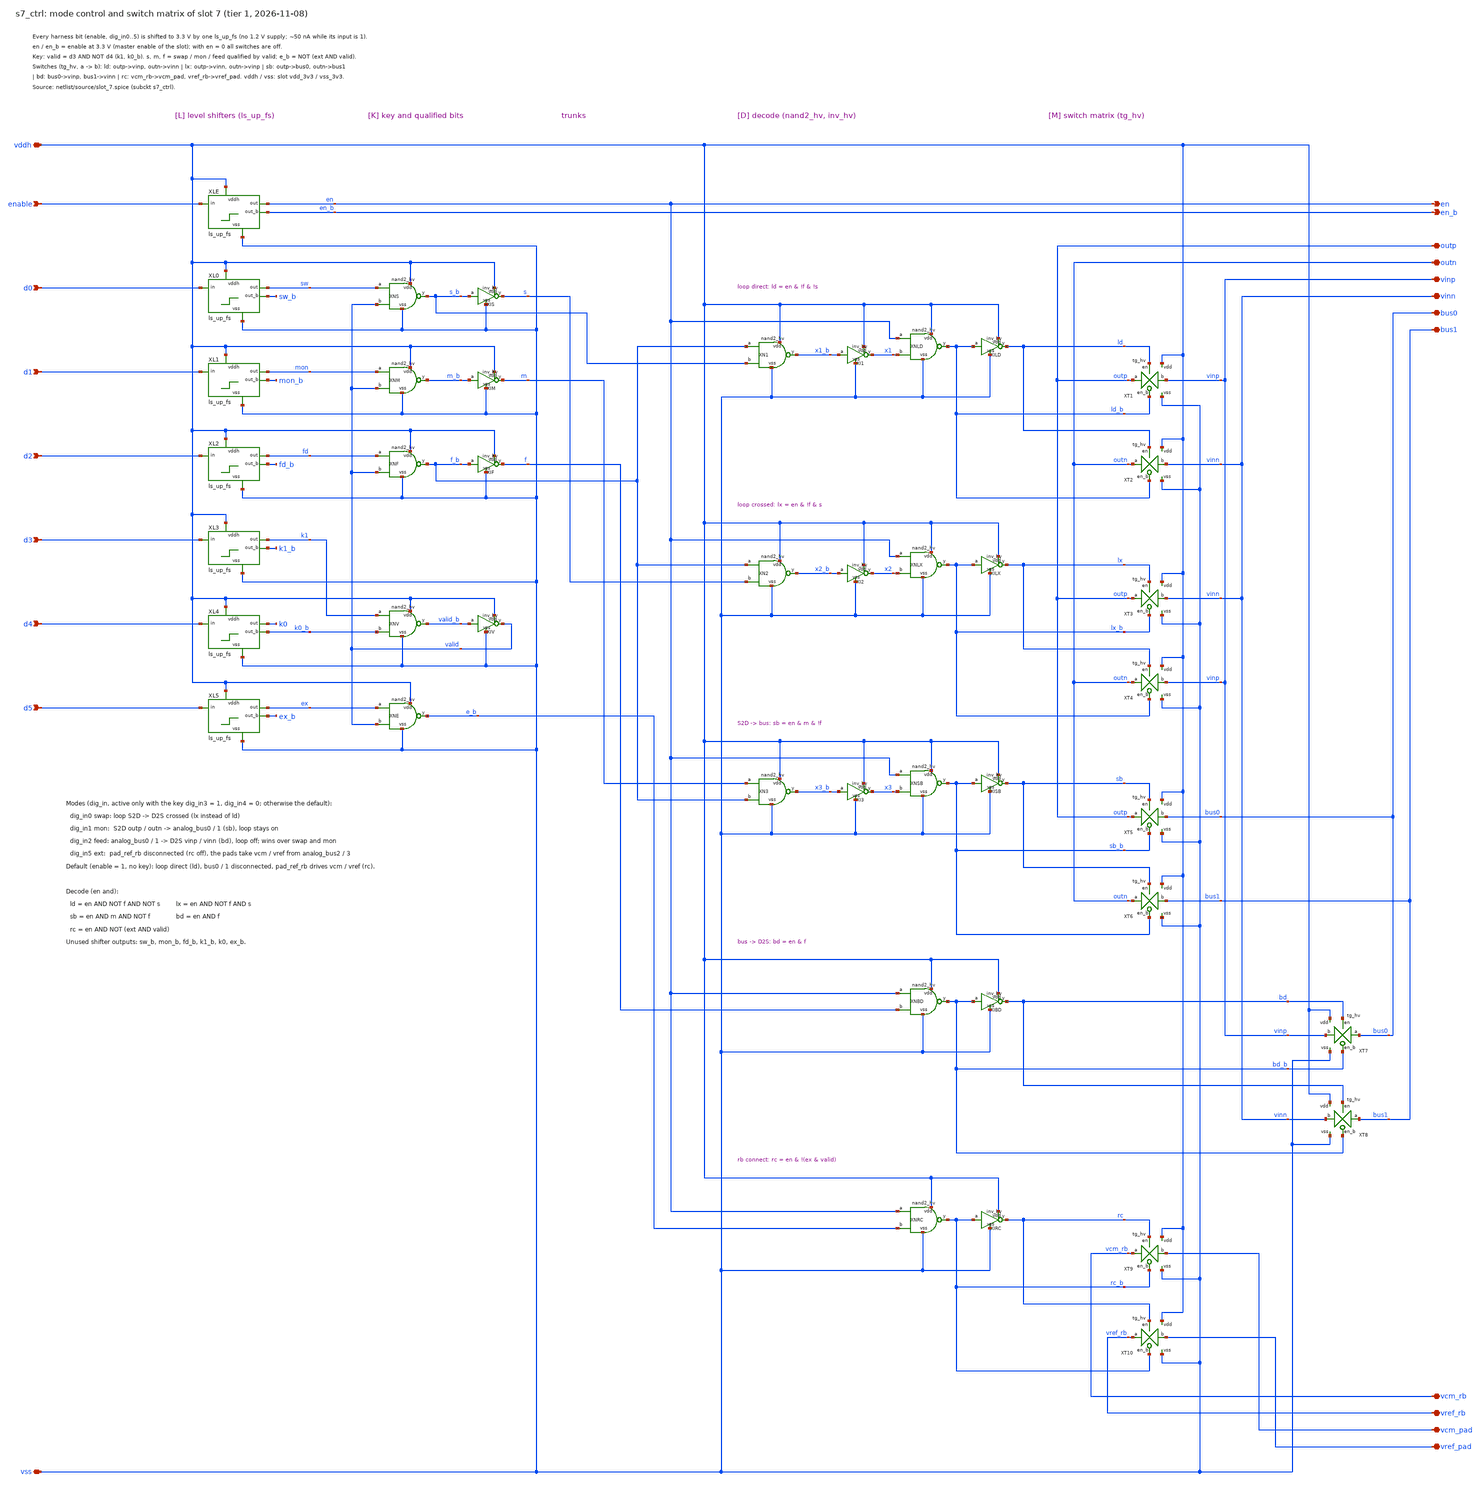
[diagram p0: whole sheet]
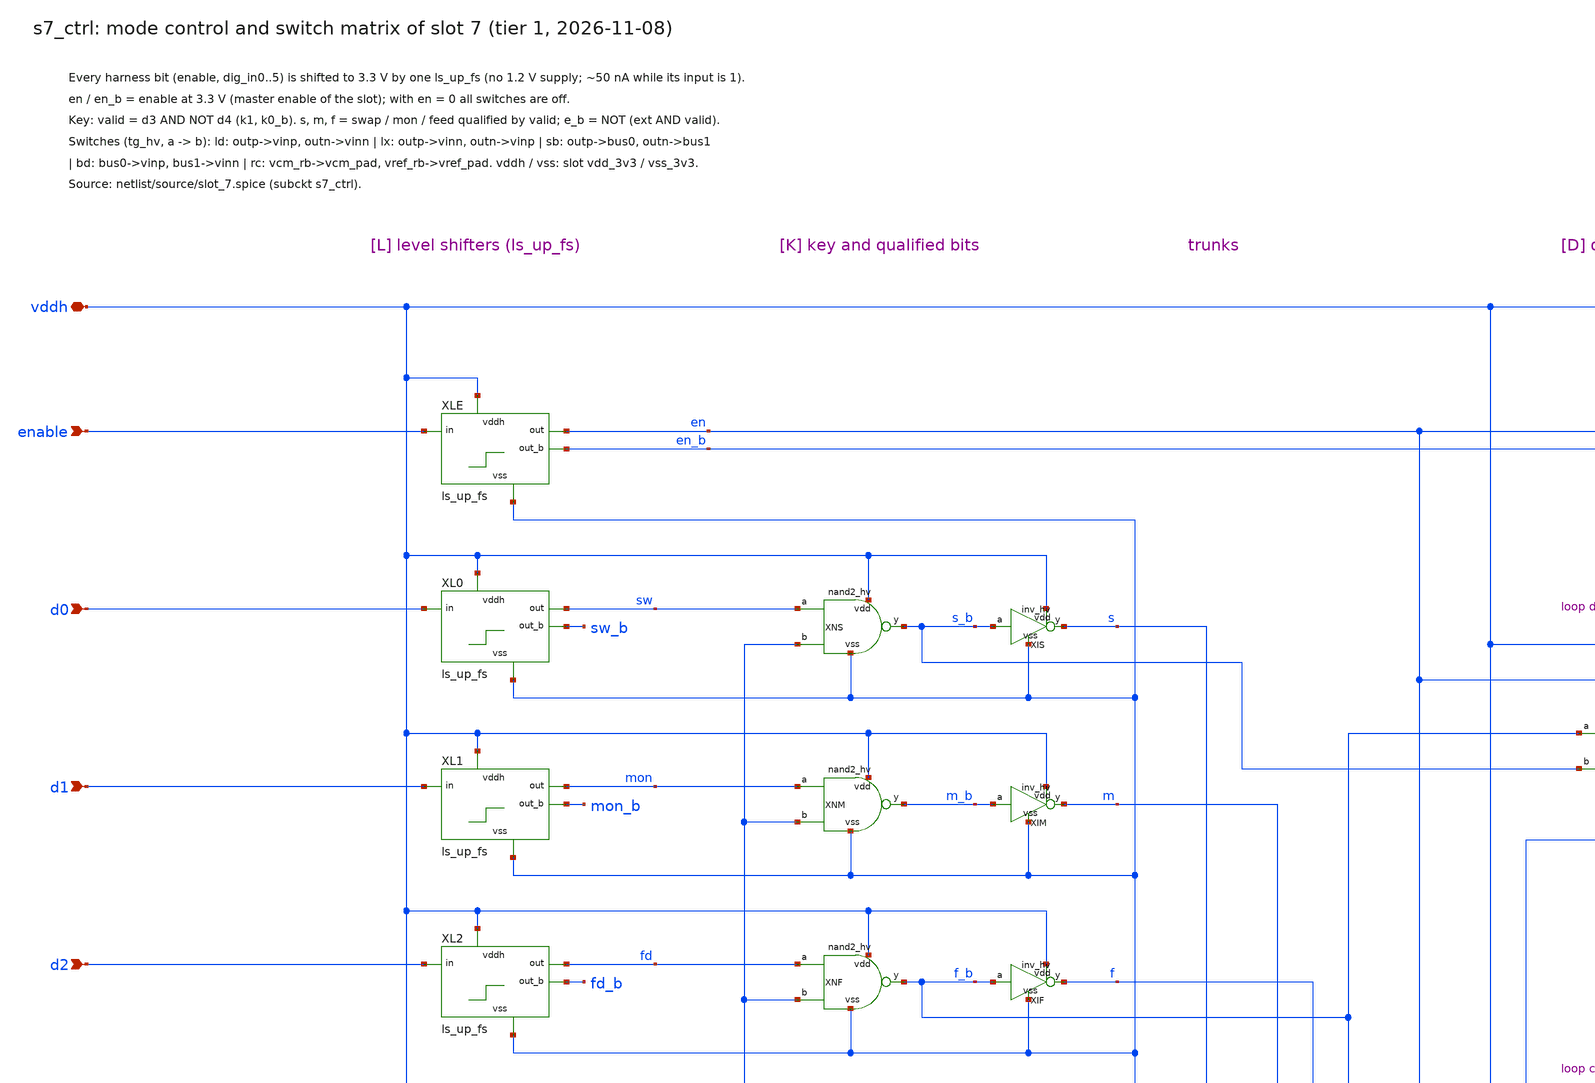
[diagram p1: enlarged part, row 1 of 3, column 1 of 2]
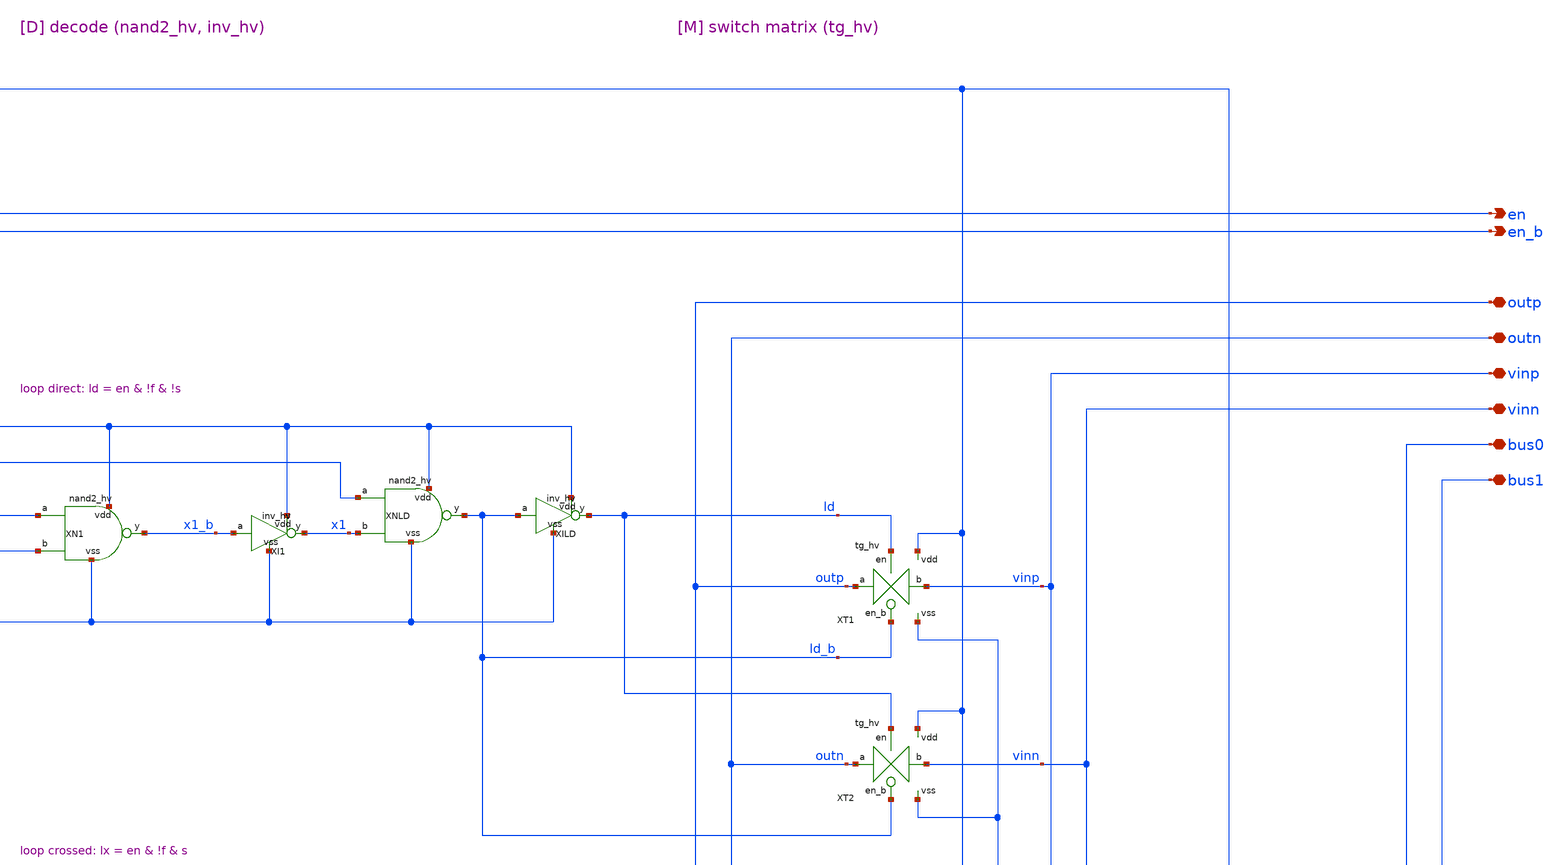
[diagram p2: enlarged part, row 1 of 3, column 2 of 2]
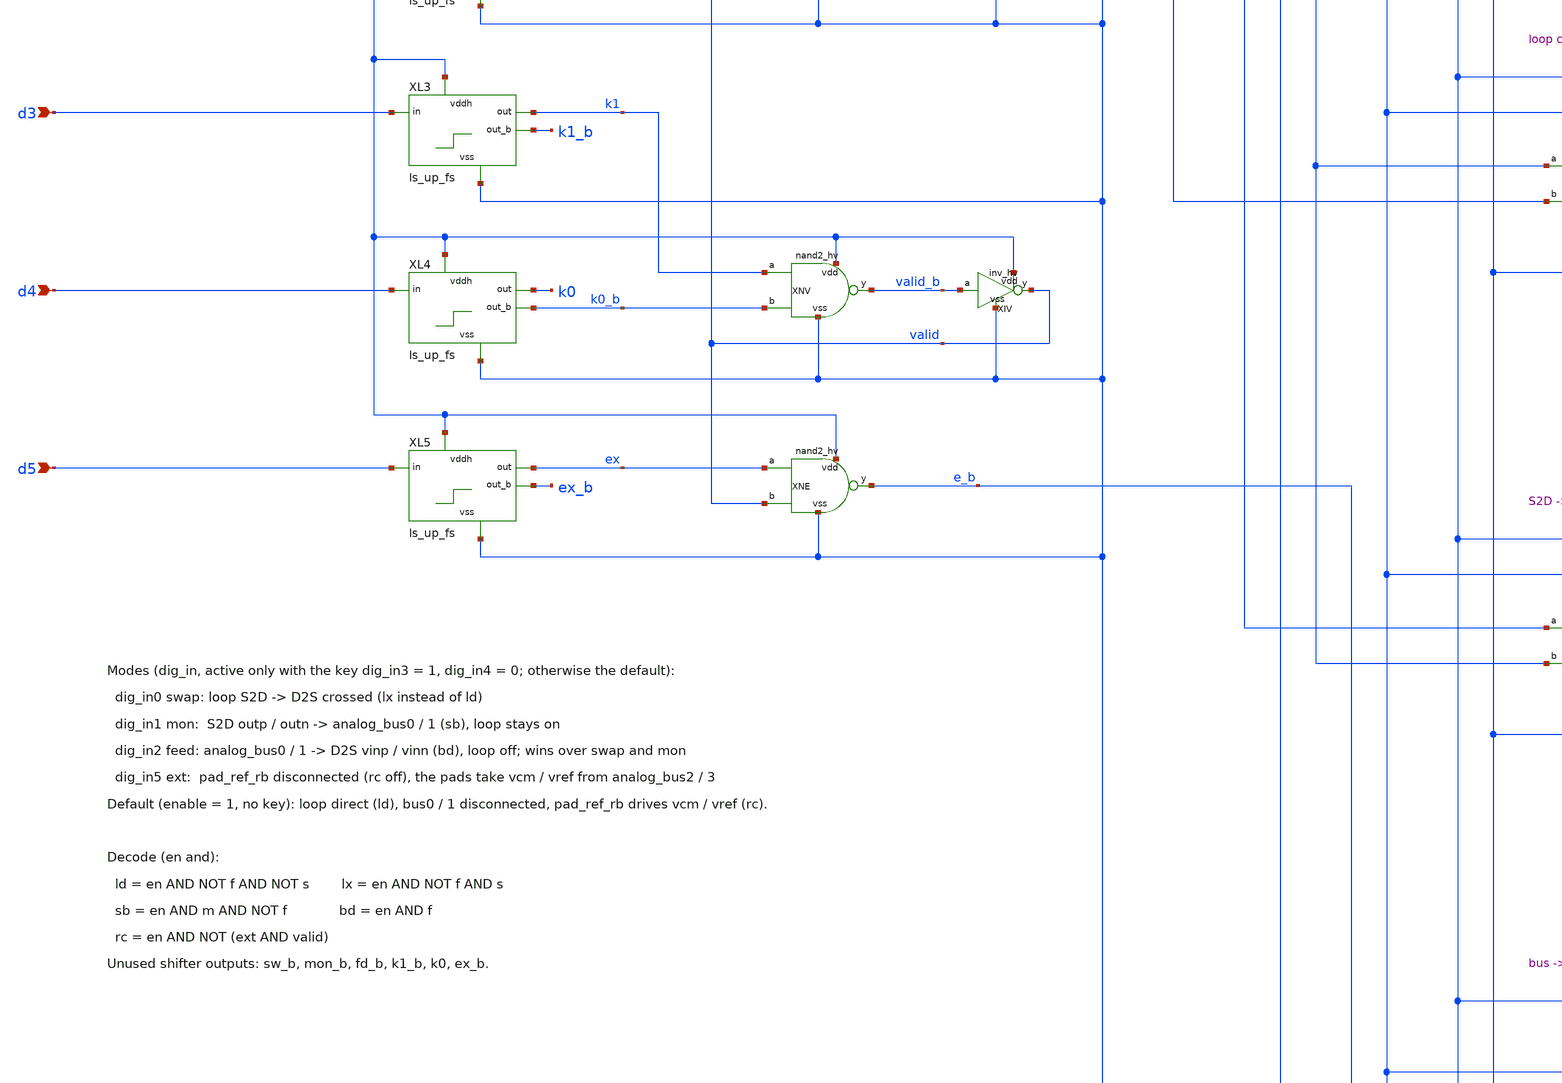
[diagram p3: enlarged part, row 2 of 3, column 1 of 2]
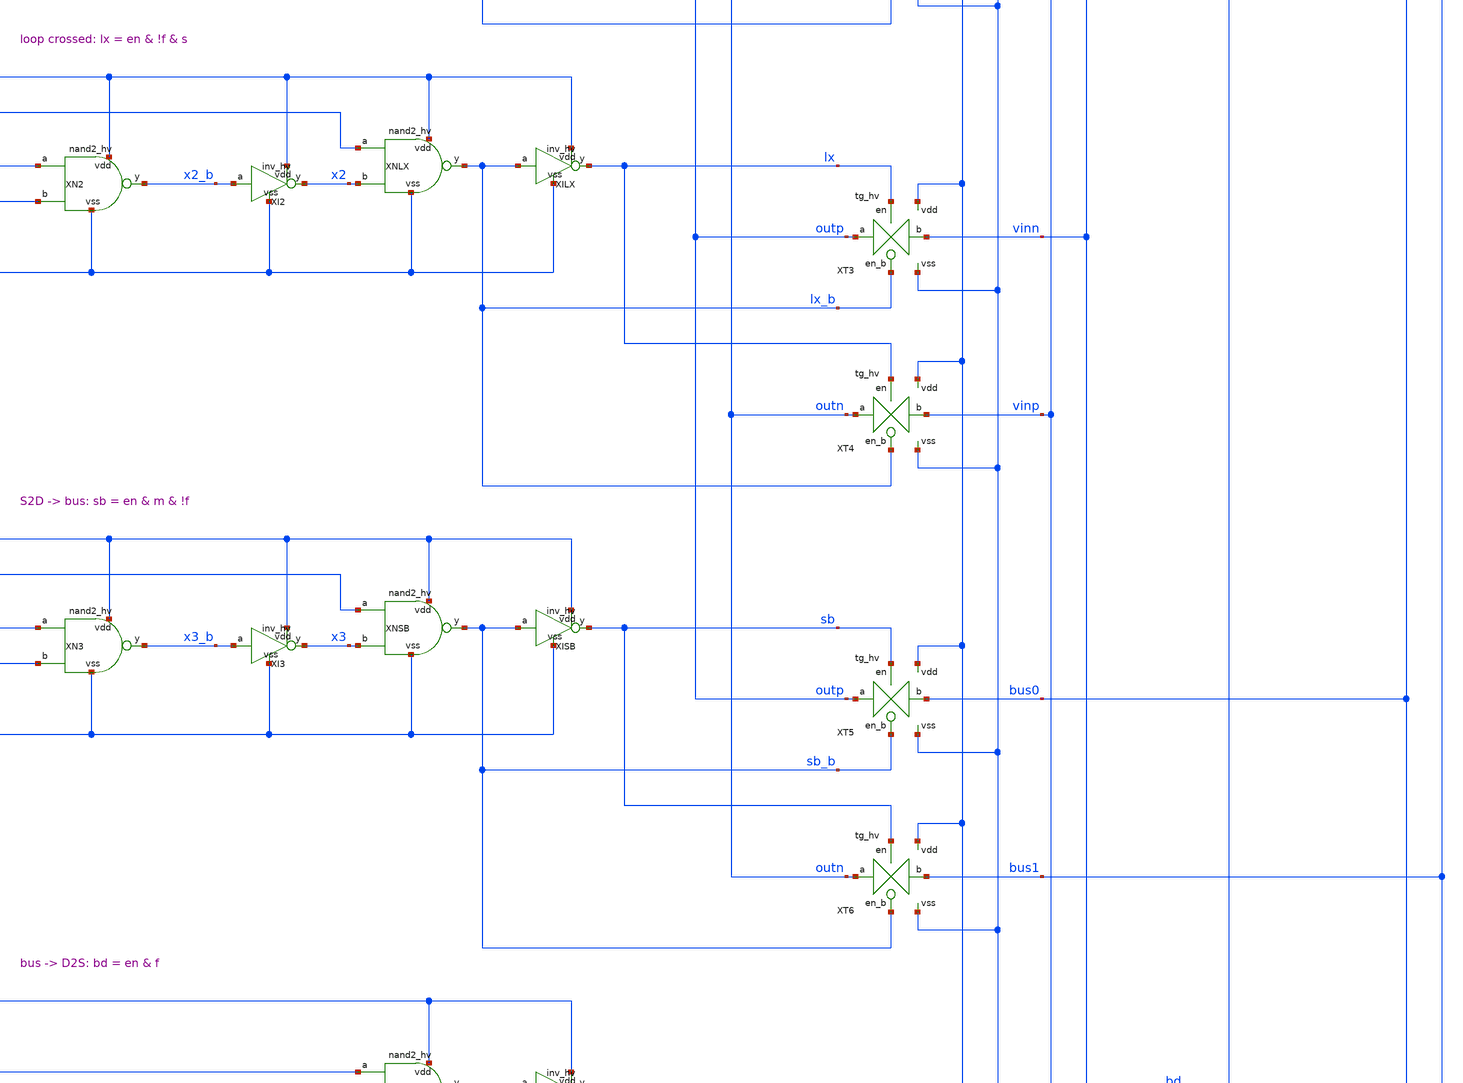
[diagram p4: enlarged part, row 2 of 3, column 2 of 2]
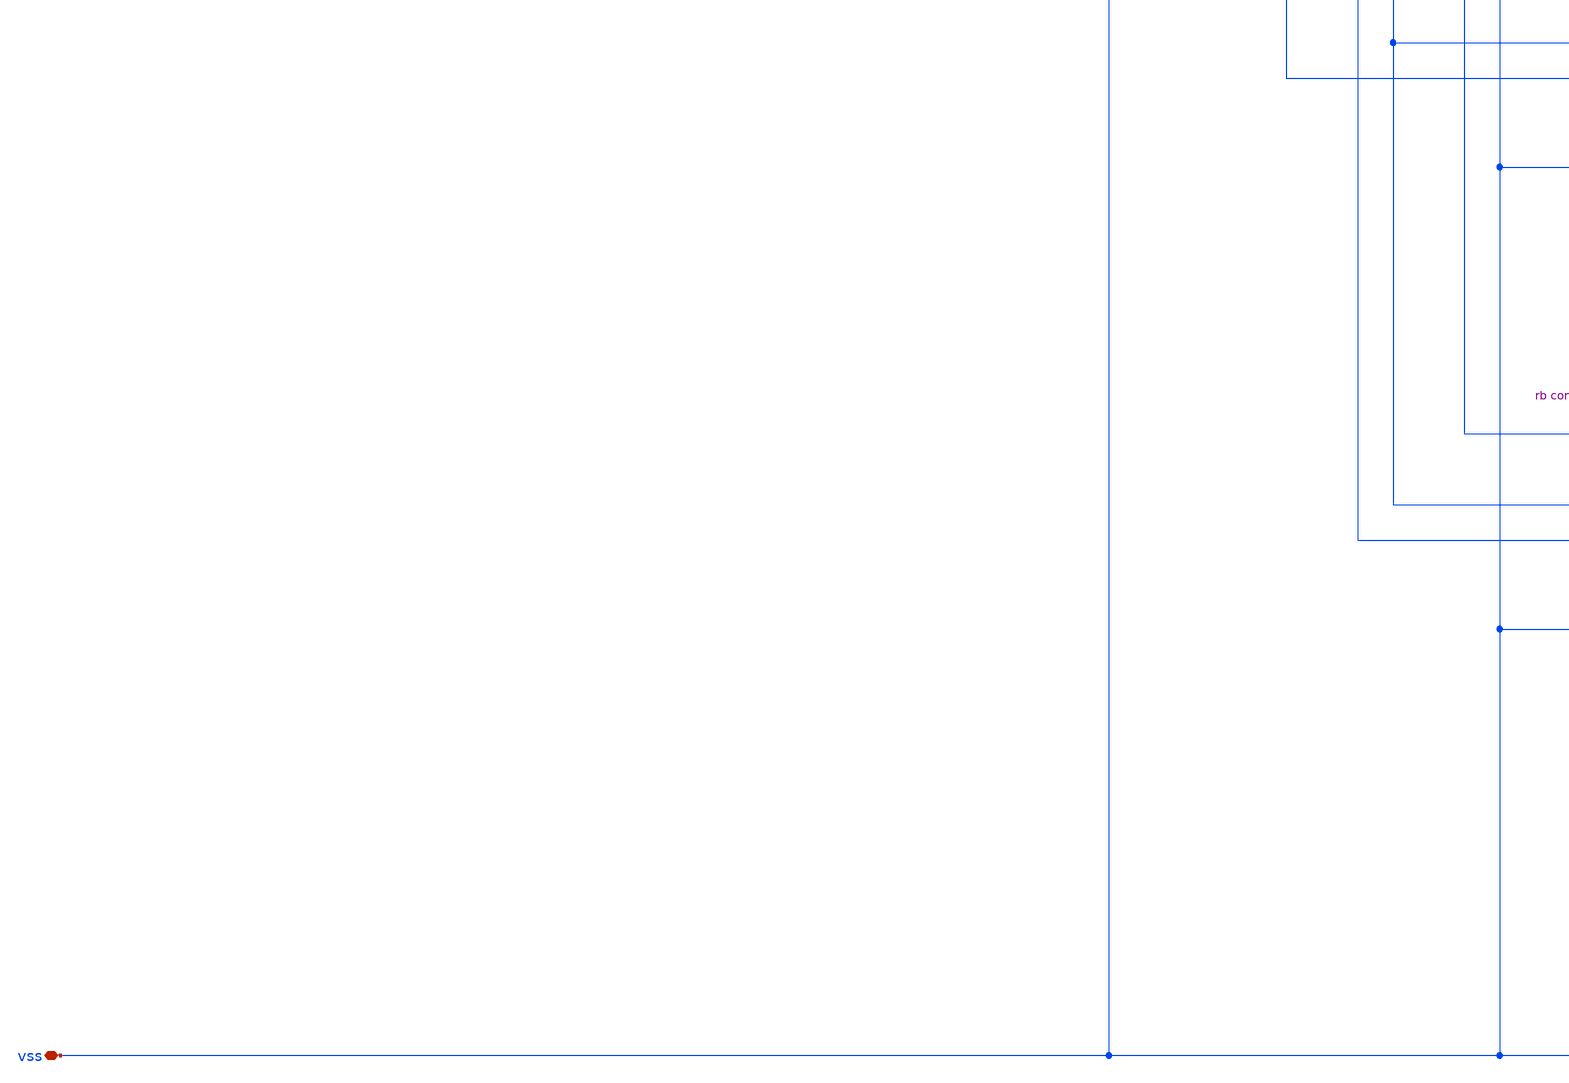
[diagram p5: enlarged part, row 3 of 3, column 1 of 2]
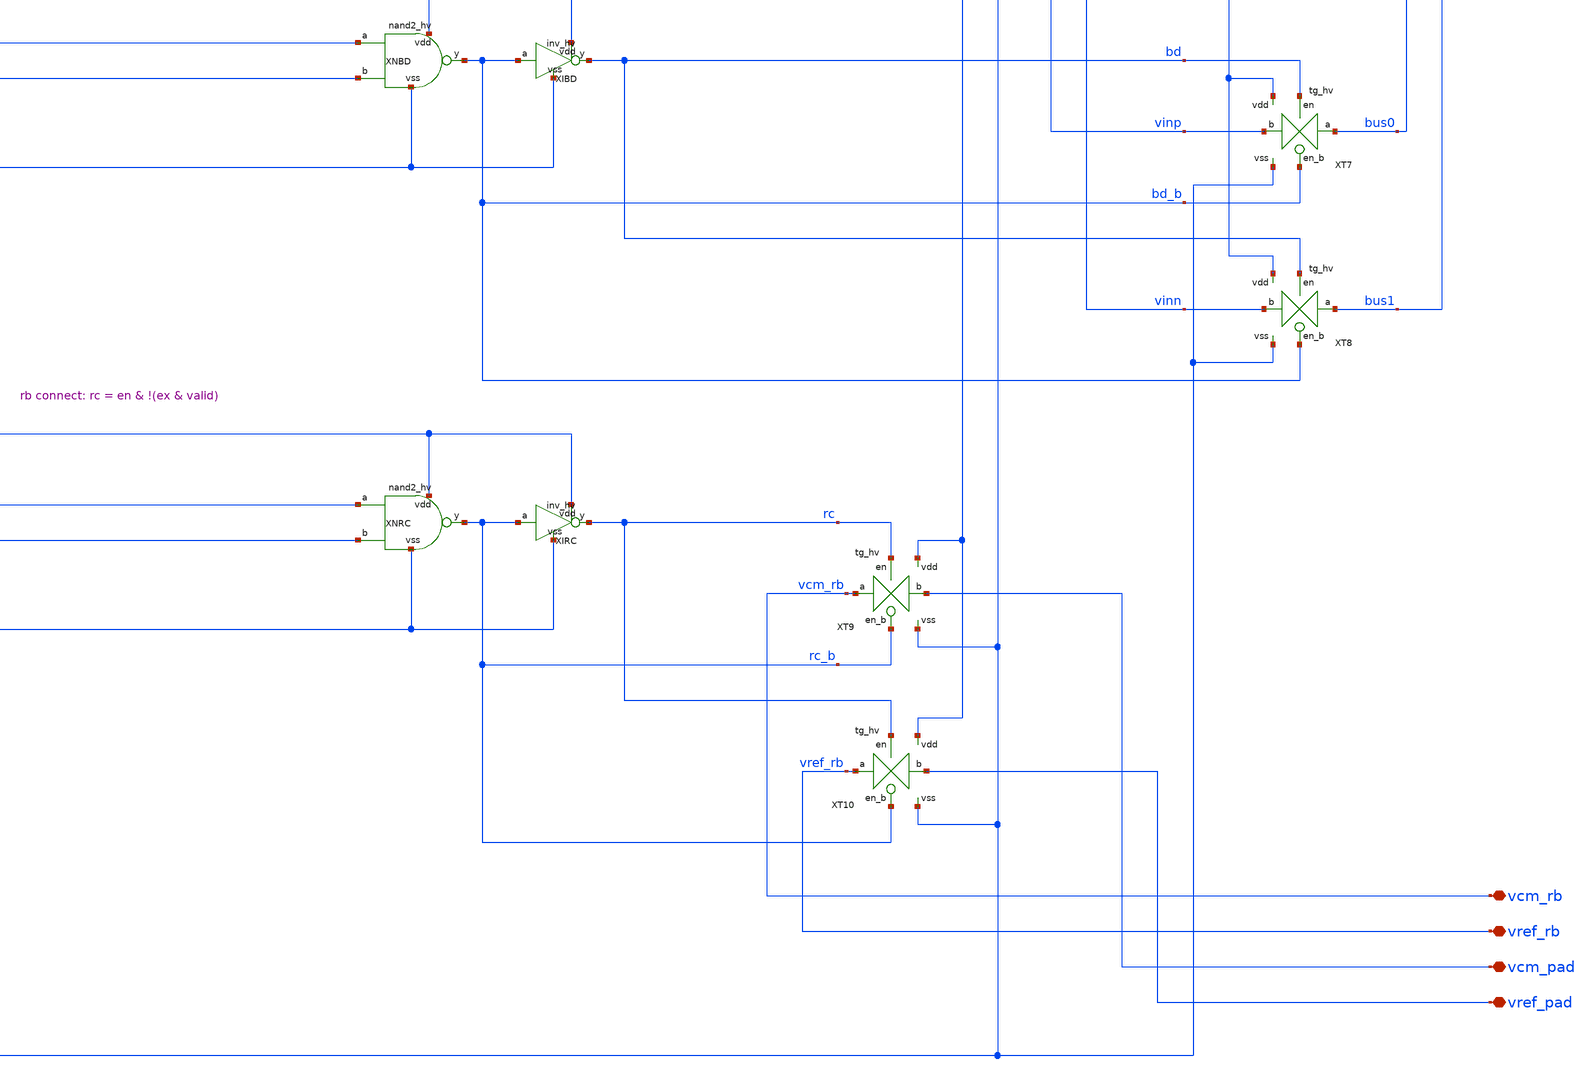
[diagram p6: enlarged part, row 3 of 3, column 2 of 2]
** sch_path: macros/slot_7/schematic/xschem/s7_ctrl.sch
**.subckt s7_ctrl vddh vss enable d0 d1 d2 d3 d4 d5 en en_b outp outn vinp vinn bus0 bus1 vcm_rb
*+ vref_rb vcm_pad vref_pad
*.iopin vddh
*.iopin vss
*.ipin enable
*.ipin d0
*.ipin d1
*.ipin d2
*.ipin d3
*.ipin d4
*.ipin d5
*.opin en
*.opin en_b
*.iopin outp
*.iopin outn
*.iopin vinp
*.iopin vinn
*.iopin bus0
*.iopin bus1
*.iopin vcm_rb
*.iopin vref_rb
*.iopin vcm_pad
*.iopin vref_pad
XLE vddh vss enable en en_b ls_up_fs
XL0 vddh vss d0 sw sw_b ls_up_fs
XL1 vddh vss d1 mon mon_b ls_up_fs
XL2 vddh vss d2 fd fd_b ls_up_fs
XL3 vddh vss d3 k1 k1_b ls_up_fs
XL4 vddh vss d4 k0 k0_b ls_up_fs
XL5 vddh vss d5 ex ex_b ls_up_fs
XNS vddh vss sw valid s_b nand2_hv
XIS vddh vss s_b s inv_hv
XNM vddh vss mon valid m_b nand2_hv
XIM vddh vss m_b m inv_hv
XNF vddh vss fd valid f_b nand2_hv
XIF vddh vss f_b f inv_hv
XNE vddh vss ex valid e_b nand2_hv
XNV vddh vss k1 k0_b valid_b nand2_hv
XIV vddh vss valid_b valid inv_hv
XN1 vddh vss f_b s_b x1_b nand2_hv
XI1 vddh vss x1_b x1 inv_hv
XNLD vddh vss en x1 ld_b nand2_hv
XILD vddh vss ld_b ld inv_hv
XN2 vddh vss f_b s x2_b nand2_hv
XI2 vddh vss x2_b x2 inv_hv
XNLX vddh vss en x2 lx_b nand2_hv
XILX vddh vss lx_b lx inv_hv
XN3 vddh vss m f_b x3_b nand2_hv
XI3 vddh vss x3_b x3 inv_hv
XNSB vddh vss en x3 sb_b nand2_hv
XISB vddh vss sb_b sb inv_hv
XNBD vddh vss en f bd_b nand2_hv
XIBD vddh vss bd_b bd inv_hv
XNRC vddh vss en e_b rc_b nand2_hv
XIRC vddh vss rc_b rc inv_hv
XT1 vddh vss ld ld_b outp vinp tg_hv
XT2 vddh vss ld ld_b outn vinn tg_hv
XT3 vddh vss lx lx_b outp vinn tg_hv
XT4 vddh vss lx lx_b outn vinp tg_hv
XT5 vddh vss sb sb_b outp bus0 tg_hv
XT6 vddh vss sb sb_b outn bus1 tg_hv
XT7 vddh vss bd bd_b bus0 vinp tg_hv
XT8 vddh vss bd bd_b bus1 vinn tg_hv
XT9 vddh vss rc rc_b vcm_rb vcm_pad tg_hv
XT10 vddh vss rc rc_b vref_rb vref_pad tg_hv
**.ends

* expanding   symbol:  ls_up_fs.sym # of pins=5
** sym_path: macros/en_ctrl_3v3/schematic/xschem/ls_up_fs.sym
** sch_path: macros/en_ctrl_3v3/schematic/xschem/ls_up_fs.sch
.subckt ls_up_fs vddh vss in out out_b
*.iopin vddh
*.iopin vss
*.ipin in
*.opin out
*.opin out_b
XN1 x in vss vss sg13_hv_nmos w=1u l=0.45u ng=1 m=1 mm_ok=1
XPL10 l9 in vddh vddh sg13_hv_pmos w=0.3u l=20u ng=1 m=1 mm_ok=1
XPL9 l8 in l9 vddh sg13_hv_pmos w=0.3u l=20u ng=1 m=1 mm_ok=1
XPL8 l7 in l8 vddh sg13_hv_pmos w=0.3u l=20u ng=1 m=1 mm_ok=1
XPL7 l6 in l7 vddh sg13_hv_pmos w=0.3u l=20u ng=1 m=1 mm_ok=1
XPL6 l5 in l6 vddh sg13_hv_pmos w=0.3u l=20u ng=1 m=1 mm_ok=1
XPL5 l4 in l5 vddh sg13_hv_pmos w=0.3u l=20u ng=1 m=1 mm_ok=1
XPL4 l3 in l4 vddh sg13_hv_pmos w=0.3u l=20u ng=1 m=1 mm_ok=1
XPL3 l2 in l3 vddh sg13_hv_pmos w=0.3u l=20u ng=1 m=1 mm_ok=1
XPL2 l1 in l2 vddh sg13_hv_pmos w=0.3u l=20u ng=1 m=1 mm_ok=1
XPL1 x in l1 vddh sg13_hv_pmos w=0.3u l=20u ng=1 m=1 mm_ok=1
XPF x y vddh vddh sg13_hv_pmos w=0.3u l=5u ng=1 m=1 mm_ok=1
XI1 vddh vss x y inv_hv
XI2 vddh vss y out_b inv_hv
XI3 vddh vss out_b out inv_hv
.ends


* expanding   symbol:  nand2_hv.sym # of pins=5
** sym_path: macros/hv_logic/schematic/xschem/nand2_hv.sym
** sch_path: macros/hv_logic/schematic/xschem/nand2_hv.sch
.subckt nand2_hv vdd vss a b y
*.iopin vdd
*.iopin vss
*.ipin a
*.ipin b
*.opin y
XPA y a vdd vdd sg13_hv_pmos w=1u l=0.45u ng=1 m=1 mm_ok=1
XPB y b vdd vdd sg13_hv_pmos w=1u l=0.45u ng=1 m=1 mm_ok=1
XNA y a n1 vss sg13_hv_nmos w=1u l=0.45u ng=1 m=1 mm_ok=1
XNB n1 b vss vss sg13_hv_nmos w=1u l=0.45u ng=1 m=1 mm_ok=1
.ends


* expanding   symbol:  inv_hv.sym # of pins=4
** sym_path: macros/hv_logic/schematic/xschem/inv_hv.sym
** sch_path: macros/hv_logic/schematic/xschem/inv_hv.sch
.subckt inv_hv vdd vss a y
*.iopin vdd
*.iopin vss
*.ipin a
*.opin y
XP y a vdd vdd sg13_hv_pmos w=1u l=0.45u ng=1 m=1 mm_ok=1
XN y a vss vss sg13_hv_nmos w=1u l=0.45u ng=1 m=1 mm_ok=1
.ends


* expanding   symbol:  tg_hv.sym # of pins=6
** sym_path: macros/hv_logic/schematic/xschem/tg_hv.sym
** sch_path: macros/hv_logic/schematic/xschem/tg_hv.sch
.subckt tg_hv vdd vss en en_b a b
*.iopin vdd
*.iopin vss
*.ipin en
*.ipin en_b
*.iopin a
*.iopin b
XN a en b vss sg13_hv_nmos w=1u l=0.45u ng=1 m=1 mm_ok=1
XP a en_b b vdd sg13_hv_pmos w=1u l=0.45u ng=1 m=1 mm_ok=1
.ends

.end
